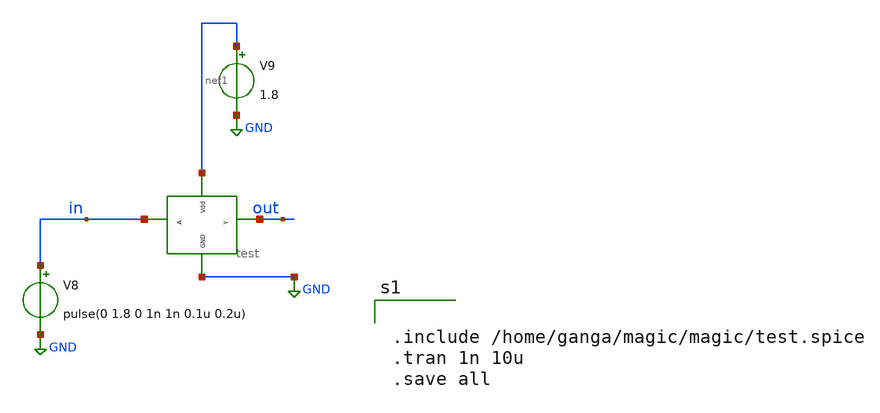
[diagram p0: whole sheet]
** sch_path: xschem/xschemfiles/inv_tb.sch
**.subckt inv_tb
V9 net1 GND 1.8
V8 in GND pulse(0 1.8 0 1n 1n 0.1u 0.2u)
x1 in out GND net1 test
**** begin user architecture code


.include /home/ganga/magic/magic/test.spice
.tran 1n 10u
.save all



** opencircuitdesign pdks install
.lib $::SKYWATER_MODELS/sky130.lib.spice tt


**** end user architecture code
**.ends
.GLOBAL GND
.end
